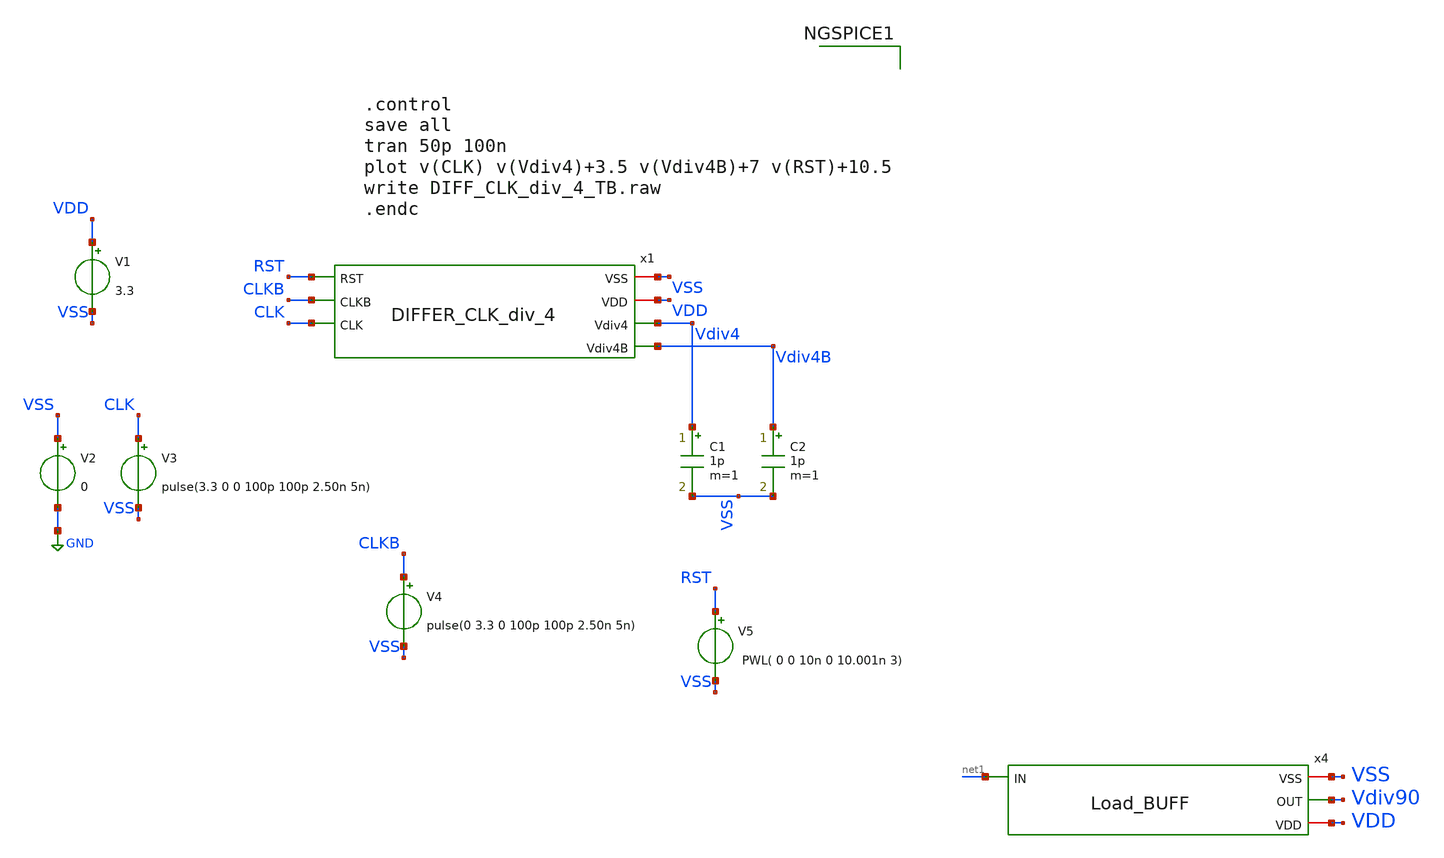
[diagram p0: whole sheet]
** sch_path: Clock_Generator_PAKISTAN_02/xschem/DIFF_CLK_div_4_TB.sch
**.subckt DIFF_CLK_div_4_TB
V1 VDD VSS 3.3
V2 VSS GND 0
V3 CLK VSS pulse(3.3 0 0 100p 100p 2.50n 5n)
C1 Vdiv4 VSS 1p m=1
C2 Vdiv4B VSS 1p m=1
V5 RST VSS PWL( 0 0 10n 0 10.001n 3)
V4 CLKB VSS pulse(0 3.3 0 100p 100p 2.50n 5n)
x1 VSS VDD RST Vdiv4 Vdiv4B CLKB CLK DIFFER_CLK_div_4
x4 VSS net1 Vdiv90 VDD Load_BUFF
**** begin user architecture code

.include $::180MCU_MODELS/design.ngspice
.lib $::180MCU_MODELS/sm141064.ngspice typical




.control
save all
tran 50p 100n
plot v(CLK) v(Vdiv4)+3.5 v(Vdiv4B)+7 v(RST)+10.5
write DIFF_CLK_div_4_TB.raw
.endc


**** end user architecture code
**.ends
.GLOBAL GND
.end
